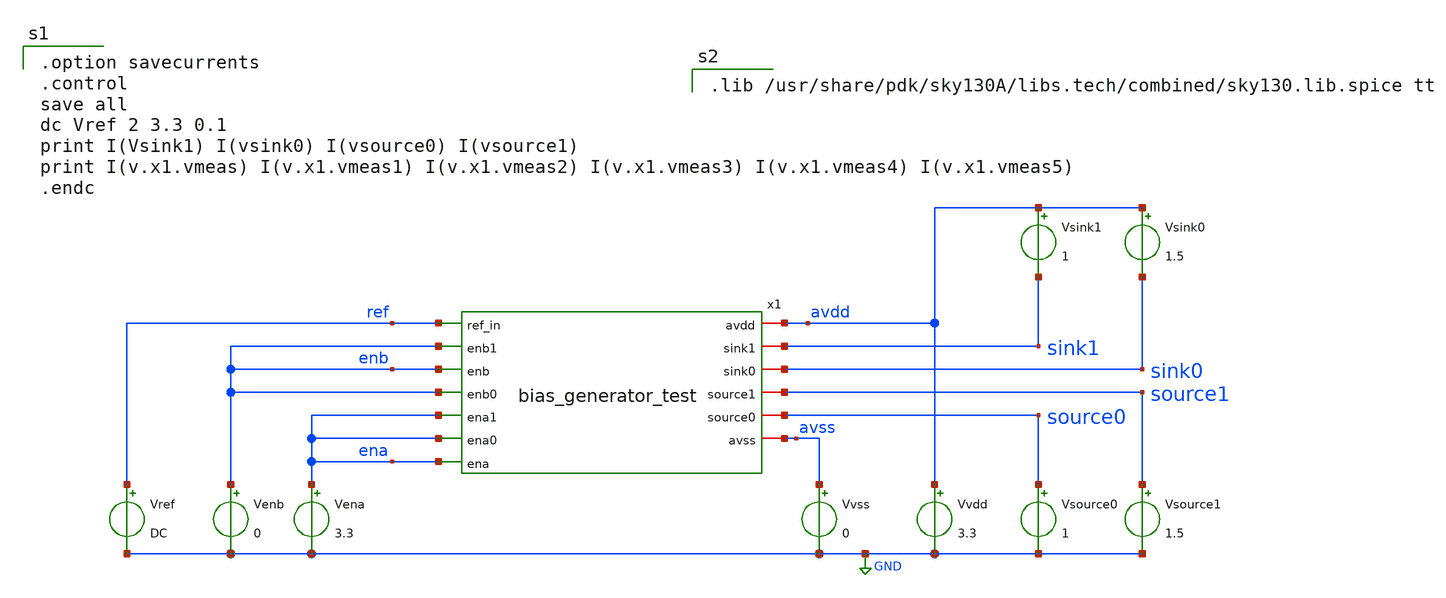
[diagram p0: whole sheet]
** sch_path: xschem/bias_generator_test_tb.sch
**.subckt bias_generator_test_tb
x1 avdd ref enb enb enb sink1 sink0 source1 source0 ena ena ena avss bias_generator_test
Vvdd avdd GND 3.3
Vvss avss GND 0
Vsource0 source0 GND 1
Vsource1 source1 GND 1.5
Vsink1 avdd sink1 1
Vsink0 avdd sink0 1.5
Vena ena GND 3.3
Venb enb GND 0
Vref ref GND DC
**** begin user architecture code

.option savecurrents
.control
save all
dc Vref 2 3.3 0.1
print I(Vsink1) I(vsink0) I(vsource0) I(vsource1)
print I(v.x1.vmeas) I(v.x1.vmeas1) I(v.x1.vmeas2) I(v.x1.vmeas3) I(v.x1.vmeas4) I(v.x1.vmeas5)
.endc


.lib /usr/share/pdk/sky130A/libs.tech/combined/sky130.lib.spice tt


**** end user architecture code
**.ends

* expanding   symbol:  bias_generator_test.sym # of pins=13
** sym_path: xschem/bias_generator_test.sym
** sch_path: xschem/bias_generator_test.sch
.subckt bias_generator_test avdd ref_in enb1 enb enb0 sink1 sink0 source1 source0 ena1 ena0 ena avss
*.ipin ref_in
*.iopin sink0
*.iopin sink1
*.iopin avss
*.ipin ena
*.iopin avdd
*.iopin source1
*.iopin source0
*.ipin ena0
*.ipin ena1
*.ipin enb
*.ipin enb0
*.ipin enb1
XR1 vresb net15 avss sky130_fd_pr__res_high_po_0p35 L=900 mult=1 m=1
XM2 net5 nbias avss avss sky130_fd_pr__nfet_g5v0d10v5 L=1 W=60 nf=1 ad='int((nf+1)/2) * W/nf * 0.29'
+ as='int((nf+2)/2) * W/nf * 0.29' pd='2*int((nf+1)/2) * (W/nf + 0.29)' ps='2*int((nf+2)/2) * (W/nf + 0.29)'
+ nrd='0.29 / W' nrs='0.29 / W' sa=0 sb=0 sd=0 mult=1 m=1
XM3 net6 nbias avss avss sky130_fd_pr__nfet_g5v0d10v5 L=1 W=3 nf=1 ad='int((nf+1)/2) * W/nf * 0.29' as='int((nf+2)/2) * W/nf * 0.29'
+ pd='2*int((nf+1)/2) * (W/nf + 0.29)' ps='2*int((nf+2)/2) * (W/nf + 0.29)' nrd='0.29 / W' nrs='0.29 / W'
+ sa=0 sb=0 sd=0 mult=1 m=1
XM5 net7 nbias avss avss sky130_fd_pr__nfet_g5v0d10v5 L=1 W=3 nf=1 ad='int((nf+1)/2) * W/nf * 0.29' as='int((nf+2)/2) * W/nf * 0.29'
+ pd='2*int((nf+1)/2) * (W/nf + 0.29)' ps='2*int((nf+2)/2) * (W/nf + 0.29)' nrd='0.29 / W' nrs='0.29 / W'
+ sa=0 sb=0 sd=0 mult=1 m=1
XM7 net8 nbias avss avss sky130_fd_pr__nfet_g5v0d10v5 L=1 W=3 nf=1 ad='int((nf+1)/2) * W/nf * 0.29' as='int((nf+2)/2) * W/nf * 0.29'
+ pd='2*int((nf+1)/2) * (W/nf + 0.29)' ps='2*int((nf+2)/2) * (W/nf + 0.29)' nrd='0.29 / W' nrs='0.29 / W'
+ sa=0 sb=0 sd=0 mult=1 m=1
XM10 net12 pbias avdd avdd sky130_fd_pr__pfet_g5v0d10v5 L=1 W=3 nf=1 ad='int((nf+1)/2) * W/nf * 0.29'
+ as='int((nf+2)/2) * W/nf * 0.29' pd='2*int((nf+1)/2) * (W/nf + 0.29)' ps='2*int((nf+2)/2) * (W/nf + 0.29)'
+ nrd='0.29 / W' nrs='0.29 / W' sa=0 sb=0 sd=0 mult=1 m=1
XM13 net14 pbias avdd avdd sky130_fd_pr__pfet_g5v0d10v5 L=1 W=3 nf=1 ad='int((nf+1)/2) * W/nf * 0.29'
+ as='int((nf+2)/2) * W/nf * 0.29' pd='2*int((nf+1)/2) * (W/nf + 0.29)' ps='2*int((nf+2)/2) * (W/nf + 0.29)'
+ nrd='0.29 / W' nrs='0.29 / W' sa=0 sb=0 sd=0 mult=1 m=1
XM15 net13 pbias avdd avdd sky130_fd_pr__pfet_g5v0d10v5 L=1 W=3 nf=1 ad='int((nf+1)/2) * W/nf * 0.29'
+ as='int((nf+2)/2) * W/nf * 0.29' pd='2*int((nf+1)/2) * (W/nf + 0.29)' ps='2*int((nf+2)/2) * (W/nf + 0.29)'
+ nrd='0.29 / W' nrs='0.29 / W' sa=0 sb=0 sd=0 mult=1 m=1
XM18 net2 enb0 vsrc0 avdd sky130_fd_pr__pfet_g5v0d10v5 L=1 W=3 nf=1 ad='int((nf+1)/2) * W/nf * 0.29'
+ as='int((nf+2)/2) * W/nf * 0.29' pd='2*int((nf+1)/2) * (W/nf + 0.29)' ps='2*int((nf+2)/2) * (W/nf + 0.29)'
+ nrd='0.29 / W' nrs='0.29 / W' sa=0 sb=0 sd=0 mult=1 m=1
XM19 net1 enb1 vsrc1 avdd sky130_fd_pr__pfet_g5v0d10v5 L=1 W=3 nf=1 ad='int((nf+1)/2) * W/nf * 0.29'
+ as='int((nf+2)/2) * W/nf * 0.29' pd='2*int((nf+1)/2) * (W/nf + 0.29)' ps='2*int((nf+2)/2) * (W/nf + 0.29)'
+ nrd='0.29 / W' nrs='0.29 / W' sa=0 sb=0 sd=0 mult=1 m=1
XM20 net9 enb pbias avdd sky130_fd_pr__pfet_g5v0d10v5 L=1 W=3 nf=1 ad='int((nf+1)/2) * W/nf * 0.29' as='int((nf+2)/2) * W/nf * 0.29'
+ pd='2*int((nf+1)/2) * (W/nf + 0.29)' ps='2*int((nf+2)/2) * (W/nf + 0.29)' nrd='0.29 / W' nrs='0.29 / W'
+ sa=0 sb=0 sd=0 mult=1 m=1
Vmeas net9 net10 0
.save i(vmeas)
Vmeas1 sink0 net3 0
.save i(vmeas1)
Vmeas2 sink1 net4 0
.save i(vmeas2)
Vmeas3 net2 source0 0
.save i(vmeas3)
Vmeas4 net1 source1 0
.save i(vmeas4)
Vmeas5 pcasc net15 0
.save i(vmeas5)
XM4 vresb ena nbias avss sky130_fd_pr__nfet_g5v0d10v5 L=1 W=60 nf=1 ad='int((nf+1)/2) * W/nf * 0.29'
+ as='int((nf+2)/2) * W/nf * 0.29' pd='2*int((nf+1)/2) * (W/nf + 0.29)' ps='2*int((nf+2)/2) * (W/nf + 0.29)'
+ nrd='0.29 / W' nrs='0.29 / W' sa=0 sb=0 sd=0 mult=1 m=1
XM16 net4 ena1 vsnk1 avss sky130_fd_pr__nfet_g5v0d10v5 L=1 W=3 nf=1 ad='int((nf+1)/2) * W/nf * 0.29'
+ as='int((nf+2)/2) * W/nf * 0.29' pd='2*int((nf+1)/2) * (W/nf + 0.29)' ps='2*int((nf+2)/2) * (W/nf + 0.29)'
+ nrd='0.29 / W' nrs='0.29 / W' sa=0 sb=0 sd=0 mult=1 m=1
XM17 net3 ena0 vsnk0 avss sky130_fd_pr__nfet_g5v0d10v5 L=1 W=3 nf=1 ad='int((nf+1)/2) * W/nf * 0.29'
+ as='int((nf+2)/2) * W/nf * 0.29' pd='2*int((nf+1)/2) * (W/nf + 0.29)' ps='2*int((nf+2)/2) * (W/nf + 0.29)'
+ nrd='0.29 / W' nrs='0.29 / W' sa=0 sb=0 sd=0 mult=1 m=1
XM1 nbias nbias net5 avss sky130_fd_pr__nfet_05v0_nvt L=1 W=60 nf=1 ad='int((nf+1)/2) * W/nf * 0.29'
+ as='int((nf+2)/2) * W/nf * 0.29' pd='2*int((nf+1)/2) * (W/nf + 0.29)' ps='2*int((nf+2)/2) * (W/nf + 0.29)'
+ nrd='0.29 / W' nrs='0.29 / W' sa=0 sb=0 sd=0 mult=1 m=1
XM6 net11 nbias net6 avss sky130_fd_pr__nfet_05v0_nvt L=1 W=3 nf=1 ad='int((nf+1)/2) * W/nf * 0.29' as='int((nf+2)/2) * W/nf * 0.29'
+ pd='2*int((nf+1)/2) * (W/nf + 0.29)' ps='2*int((nf+2)/2) * (W/nf + 0.29)' nrd='0.29 / W' nrs='0.29 / W'
+ sa=0 sb=0 sd=0 mult=1 m=1
XM8 vsnk0 nbias net7 avss sky130_fd_pr__nfet_05v0_nvt L=1 W=3 nf=1 ad='int((nf+1)/2) * W/nf * 0.29' as='int((nf+2)/2) * W/nf * 0.29'
+ pd='2*int((nf+1)/2) * (W/nf + 0.29)' ps='2*int((nf+2)/2) * (W/nf + 0.29)' nrd='0.29 / W' nrs='0.29 / W'
+ sa=0 sb=0 sd=0 mult=1 m=1
XM9 vsnk1 nbias net8 avss sky130_fd_pr__nfet_05v0_nvt L=1 W=3 nf=1 ad='int((nf+1)/2) * W/nf * 0.29' as='int((nf+2)/2) * W/nf * 0.29'
+ pd='2*int((nf+1)/2) * (W/nf + 0.29)' ps='2*int((nf+2)/2) * (W/nf + 0.29)' nrd='0.29 / W' nrs='0.29 / W'
+ sa=0 sb=0 sd=0 mult=1 m=1
XM12 net10 ena net11 avss sky130_fd_pr__nfet_g5v0d10v5 L=1 W=3 nf=1 ad='int((nf+1)/2) * W/nf * 0.29'
+ as='int((nf+2)/2) * W/nf * 0.29' pd='2*int((nf+1)/2) * (W/nf + 0.29)' ps='2*int((nf+2)/2) * (W/nf + 0.29)'
+ nrd='0.29 / W' nrs='0.29 / W' sa=0 sb=0 sd=0 mult=1 m=1
XM11 pbias pcasc net12 avdd sky130_fd_pr__pfet_g5v0d10v5 L=1 W=3 nf=1 ad='int((nf+1)/2) * W/nf * 0.29'
+ as='int((nf+2)/2) * W/nf * 0.29' pd='2*int((nf+1)/2) * (W/nf + 0.29)' ps='2*int((nf+2)/2) * (W/nf + 0.29)'
+ nrd='0.29 / W' nrs='0.29 / W' sa=0 sb=0 sd=0 mult=1 m=1
XM14 vsrc0 pcasc net14 avdd sky130_fd_pr__pfet_g5v0d10v5 L=1 W=3 nf=1 ad='int((nf+1)/2) * W/nf * 0.29'
+ as='int((nf+2)/2) * W/nf * 0.29' pd='2*int((nf+1)/2) * (W/nf + 0.29)' ps='2*int((nf+2)/2) * (W/nf + 0.29)'
+ nrd='0.29 / W' nrs='0.29 / W' sa=0 sb=0 sd=0 mult=1 m=1
XM21 vsrc1 pcasc net13 avdd sky130_fd_pr__pfet_g5v0d10v5 L=1 W=3 nf=1 ad='int((nf+1)/2) * W/nf * 0.29'
+ as='int((nf+2)/2) * W/nf * 0.29' pd='2*int((nf+1)/2) * (W/nf + 0.29)' ps='2*int((nf+2)/2) * (W/nf + 0.29)'
+ nrd='0.29 / W' nrs='0.29 / W' sa=0 sb=0 sd=0 mult=1 m=1
XR2 pcasc ref_in avss sky130_fd_pr__res_high_po_0p35 L=1500 mult=1 m=1
.ends

.GLOBAL GND
.end
